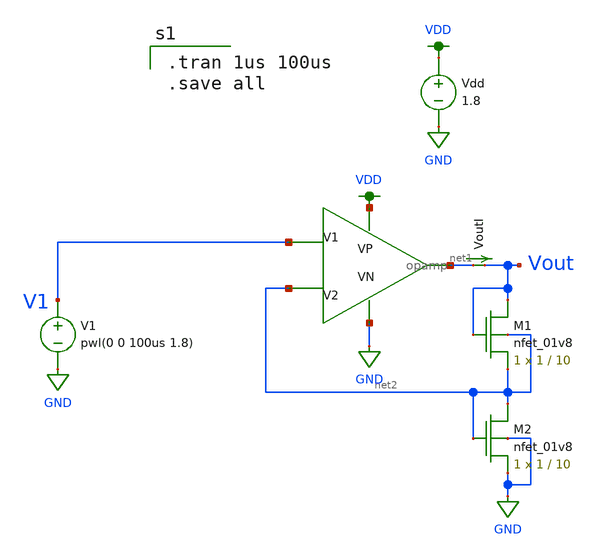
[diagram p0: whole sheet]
** sch_path: schematics/opamp_testbench.sch
**.subckt opamp_testbench
Vdd VDD GND 1.8
V1 V1 GND pwl(0 0 100us 1.8)
X1 V1 net2 VDD GND net1 opamp
VoutI net1 Vout 0
.save i(vouti)
XM1 Vout Vout net2 net2 sky130_fd_pr__nfet_01v8 L=10 W=1 nf=1 ad='int((nf+1)/2) * W/nf * 0.29' as='int((nf+2)/2) * W/nf * 0.29'
+ pd='2*int((nf+1)/2) * (W/nf + 0.29)' ps='2*int((nf+2)/2) * (W/nf + 0.29)' nrd='0.29 / W' nrs='0.29 / W'
+ sa=0 sb=0 sd=0 mult=1 m=1
XM2 net2 net2 GND GND sky130_fd_pr__nfet_01v8 L=10 W=1 nf=1 ad='int((nf+1)/2) * W/nf * 0.29' as='int((nf+2)/2) * W/nf * 0.29'
+ pd='2*int((nf+1)/2) * (W/nf + 0.29)' ps='2*int((nf+2)/2) * (W/nf + 0.29)' nrd='0.29 / W' nrs='0.29 / W'
+ sa=0 sb=0 sd=0 mult=1 m=1
**** begin user architecture code

.option wnflag=1
.param MC_SWITCH=0.0
.lib ~/skywater/skywater-pdk/libraries/sky130_fd_pr_ngspice/latest/models/sky130.lib.spice tt


.tran 1us 100us
.save all

**** end user architecture code
**.ends

* expanding   symbol:  /home/madvlsi/Documents/MADVLSI_final/schematics/opamp.sym # of pins=5
** sym_path: schematics/opamp.sym
** sch_path: schematics/opamp.sch
.subckt opamp V1 V2 VP VN Vout
*.ipin V1
*.ipin V2
*.opin Vout
*.iopin VP
*.iopin VN
*.iopin VP
*.iopin VN
XM1 VN net7 net2 GND sky130_fd_pr__nfet_01v8 L=l W=w nf=1 ad='int((nf+1)/2) * W/nf * 0.29' as='int((nf+2)/2) * W/nf * 0.29'
+ pd='2*int((nf+1)/2) * (W/nf + 0.29)' ps='2*int((nf+2)/2) * (W/nf + 0.29)' nrd='0.29 / W' nrs='0.29 / W'
+ sa=0 sb=0 sd=0 mult=1 m=1
XM2 VP net3 net1 VDD sky130_fd_pr__pfet_01v8 L=l W=w nf=1 ad='int((nf+1)/2) * W/nf * 0.29' as='int((nf+2)/2) * W/nf * 0.29'
+ pd='2*int((nf+1)/2) * (W/nf + 0.29)' ps='2*int((nf+2)/2) * (W/nf + 0.29)' nrd='0.29 / W' nrs='0.29 / W'
+ sa=0 sb=0 sd=0 mult=1 m=1
XM3 net1 V1 Vd VDD sky130_fd_pr__pfet_01v8 L=l W=w nf=1 ad='int((nf+1)/2) * W/nf * 0.29' as='int((nf+2)/2) * W/nf * 0.29'
+ pd='2*int((nf+1)/2) * (W/nf + 0.29)' ps='2*int((nf+2)/2) * (W/nf + 0.29)' nrd='0.29 / W' nrs='0.29 / W'
+ sa=0 sb=0 sd=0 mult=1 m=1
XM4 Vc V2 net1 VDD sky130_fd_pr__pfet_01v8 L=l W=w nf=1 ad='int((nf+1)/2) * W/nf * 0.29' as='int((nf+2)/2) * W/nf * 0.29'
+ pd='2*int((nf+1)/2) * (W/nf + 0.29)' ps='2*int((nf+2)/2) * (W/nf + 0.29)' nrd='0.29 / W' nrs='0.29 / W'
+ sa=0 sb=0 sd=0 mult=1 m=1
XM5 Va V2 net2 GND sky130_fd_pr__nfet_01v8 L=l W=w nf=1 ad='int((nf+1)/2) * W/nf * 0.29' as='int((nf+2)/2) * W/nf * 0.29'
+ pd='2*int((nf+1)/2) * (W/nf + 0.29)' ps='2*int((nf+2)/2) * (W/nf + 0.29)' nrd='0.29 / W' nrs='0.29 / W'
+ sa=0 sb=0 sd=0 mult=1 m=1
XM6 net2 V1 Vb GND sky130_fd_pr__nfet_01v8 L=l W=w nf=1 ad='int((nf+1)/2) * W/nf * 0.29' as='int((nf+2)/2) * W/nf * 0.29'
+ pd='2*int((nf+1)/2) * (W/nf + 0.29)' ps='2*int((nf+2)/2) * (W/nf + 0.29)' nrd='0.29 / W' nrs='0.29 / W'
+ sa=0 sb=0 sd=0 mult=1 m=1
XM7 net3 net3 Va VDD sky130_fd_pr__pfet_01v8 L=l W=w nf=1 ad='int((nf+1)/2) * W/nf * 0.29' as='int((nf+2)/2) * W/nf * 0.29'
+ pd='2*int((nf+1)/2) * (W/nf + 0.29)' ps='2*int((nf+2)/2) * (W/nf + 0.29)' nrd='0.29 / W' nrs='0.29 / W'
+ sa=0 sb=0 sd=0 mult=1 m=1
XM8 net6 net6 Va VDD sky130_fd_pr__pfet_01v8 L=l W=w nf=1 ad='int((nf+1)/2) * W/nf * 0.29' as='int((nf+2)/2) * W/nf * 0.29'
+ pd='2*int((nf+1)/2) * (W/nf + 0.29)' ps='2*int((nf+2)/2) * (W/nf + 0.29)' nrd='0.29 / W' nrs='0.29 / W'
+ sa=0 sb=0 sd=0 mult=1 m=1
XM9 net5 net6 Vb VDD sky130_fd_pr__pfet_01v8 L=l W=w nf=1 ad='int((nf+1)/2) * W/nf * 0.29' as='int((nf+2)/2) * W/nf * 0.29'
+ pd='2*int((nf+1)/2) * (W/nf + 0.29)' ps='2*int((nf+2)/2) * (W/nf + 0.29)' nrd='0.29 / W' nrs='0.29 / W'
+ sa=0 sb=0 sd=0 mult=1 m=1
XM10 Va net3 VP VDD sky130_fd_pr__pfet_01v8 L=l W=w nf=1 ad='int((nf+1)/2) * W/nf * 0.29' as='int((nf+2)/2) * W/nf * 0.29'
+ pd='2*int((nf+1)/2) * (W/nf + 0.29)' ps='2*int((nf+2)/2) * (W/nf + 0.29)' nrd='0.29 / W' nrs='0.29 / W'
+ sa=0 sb=0 sd=0 mult=1 m=1
XM11 Vb net3 VP VDD sky130_fd_pr__pfet_01v8 L=l W=w nf=1 ad='int((nf+1)/2) * W/nf * 0.29' as='int((nf+2)/2) * W/nf * 0.29'
+ pd='2*int((nf+1)/2) * (W/nf + 0.29)' ps='2*int((nf+2)/2) * (W/nf + 0.29)' nrd='0.29 / W' nrs='0.29 / W'
+ sa=0 sb=0 sd=0 mult=1 m=1
XM12 net6 net6 Vc GND sky130_fd_pr__nfet_01v8 L=l W=w nf=1 ad='int((nf+1)/2) * W/nf * 0.29' as='int((nf+2)/2) * W/nf * 0.29'
+ pd='2*int((nf+1)/2) * (W/nf + 0.29)' ps='2*int((nf+2)/2) * (W/nf + 0.29)' nrd='0.29 / W' nrs='0.29 / W'
+ sa=0 sb=0 sd=0 mult=1 m=1
XM13 net5 net6 Vd GND sky130_fd_pr__nfet_01v8 L=l W=w nf=1 ad='int((nf+1)/2) * W/nf * 0.29' as='int((nf+2)/2) * W/nf * 0.29'
+ pd='2*int((nf+1)/2) * (W/nf + 0.29)' ps='2*int((nf+2)/2) * (W/nf + 0.29)' nrd='0.29 / W' nrs='0.29 / W'
+ sa=0 sb=0 sd=0 mult=1 m=1
XM14 Vc net7 VN GND sky130_fd_pr__nfet_01v8 L=l W=w nf=1 ad='int((nf+1)/2) * W/nf * 0.29' as='int((nf+2)/2) * W/nf * 0.29'
+ pd='2*int((nf+1)/2) * (W/nf + 0.29)' ps='2*int((nf+2)/2) * (W/nf + 0.29)' nrd='0.29 / W' nrs='0.29 / W'
+ sa=0 sb=0 sd=0 mult=1 m=1
XM15 Vd net7 VN GND sky130_fd_pr__nfet_01v8 L=l W=w nf=1 ad='int((nf+1)/2) * W/nf * 0.29' as='int((nf+2)/2) * W/nf * 0.29'
+ pd='2*int((nf+1)/2) * (W/nf + 0.29)' ps='2*int((nf+2)/2) * (W/nf + 0.29)' nrd='0.29 / W' nrs='0.29 / W'
+ sa=0 sb=0 sd=0 mult=1 m=1
XM16 net8 net7 net3 GND sky130_fd_pr__nfet_01v8 L=l W=w nf=1 ad='int((nf+1)/2) * W/nf * 0.29' as='int((nf+2)/2) * W/nf * 0.29'
+ pd='2*int((nf+1)/2) * (W/nf + 0.29)' ps='2*int((nf+2)/2) * (W/nf + 0.29)' nrd='0.29 / W' nrs='0.29 / W'
+ sa=0 sb=0 sd=0 mult=1 m=1
XM17 VN net7 net8 GND sky130_fd_pr__nfet_01v8 L=l W=w nf=1 ad='int((nf+1)/2) * W/nf * 0.29' as='int((nf+2)/2) * W/nf * 0.29'
+ pd='2*int((nf+1)/2) * (W/nf + 0.29)' ps='2*int((nf+2)/2) * (W/nf + 0.29)' nrd='0.29 / W' nrs='0.29 / W'
+ sa=0 sb=0 sd=0 mult=1 m=1
XM18 net8 net7 VP GND sky130_fd_pr__nfet_01v8 L=l W=w nf=1 ad='int((nf+1)/2) * W/nf * 0.29' as='int((nf+2)/2) * W/nf * 0.29'
+ pd='2*int((nf+1)/2) * (W/nf + 0.29)' ps='2*int((nf+2)/2) * (W/nf + 0.29)' nrd='0.29 / W' nrs='0.29 / W'
+ sa=0 sb=0 sd=0 mult=M m=M
XM19 net4 net3 net7 VDD sky130_fd_pr__pfet_01v8 L=l W=w nf=1 ad='int((nf+1)/2) * W/nf * 0.29' as='int((nf+2)/2) * W/nf * 0.29'
+ pd='2*int((nf+1)/2) * (W/nf + 0.29)' ps='2*int((nf+2)/2) * (W/nf + 0.29)' nrd='0.29 / W' nrs='0.29 / W'
+ sa=0 sb=0 sd=0 mult=1 m=1
XM20 VP net3 net4 VDD sky130_fd_pr__pfet_01v8 L=l W=w nf=1 ad='int((nf+1)/2) * W/nf * 0.29' as='int((nf+2)/2) * W/nf * 0.29'
+ pd='2*int((nf+1)/2) * (W/nf + 0.29)' ps='2*int((nf+2)/2) * (W/nf + 0.29)' nrd='0.29 / W' nrs='0.29 / W'
+ sa=0 sb=0 sd=0 mult=1 m=1
XM21 net4 net3 VN VDD sky130_fd_pr__pfet_01v8 L=l W=w nf=1 ad='int((nf+1)/2) * W/nf * 0.29' as='int((nf+2)/2) * W/nf * 0.29'
+ pd='2*int((nf+1)/2) * (W/nf + 0.29)' ps='2*int((nf+2)/2) * (W/nf + 0.29)' nrd='0.29 / W' nrs='0.29 / W'
+ sa=0 sb=0 sd=0 mult=M m=M
XM22 net7 net7 Vc GND sky130_fd_pr__nfet_01v8 L=l W=w nf=1 ad='int((nf+1)/2) * W/nf * 0.29' as='int((nf+2)/2) * W/nf * 0.29'
+ pd='2*int((nf+1)/2) * (W/nf + 0.29)' ps='2*int((nf+2)/2) * (W/nf + 0.29)' nrd='0.29 / W' nrs='0.29 / W'
+ sa=0 sb=0 sd=0 mult=1 m=1
**** begin user architecture code

.param M=3
.param w=3
.param l=0.6


**** end user architecture code
XM23 Vout net5 VN GND sky130_fd_pr__nfet_01v8 L=.15 W=6 nf=1 ad='int((nf+1)/2) * W/nf * 0.29' as='int((nf+2)/2) * W/nf * 0.29'
+ pd='2*int((nf+1)/2) * (W/nf + 0.29)' ps='2*int((nf+2)/2) * (W/nf + 0.29)' nrd='0.29 / W' nrs='0.29 / W'
+ sa=0 sb=0 sd=0 mult=1 m=1
XM24 Vout net5 VP VDD sky130_fd_pr__pfet_01v8 L=.15 W=12 nf=1 ad='int((nf+1)/2) * W/nf * 0.29' as='int((nf+2)/2) * W/nf * 0.29'
+ pd='2*int((nf+1)/2) * (W/nf + 0.29)' ps='2*int((nf+2)/2) * (W/nf + 0.29)' nrd='0.29 / W' nrs='0.29 / W'
+ sa=0 sb=0 sd=0 mult=1 m=1
C1 Vout net5 500f m=1
.ends

.GLOBAL GND
.GLOBAL VDD
.end
